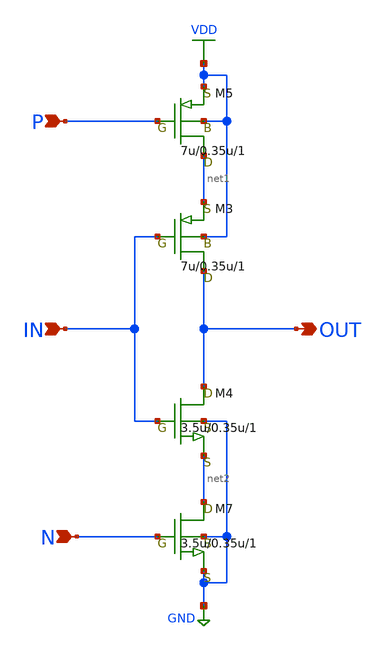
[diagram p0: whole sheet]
** sch_path: LR_hasegawa/LR_Work2/symbol/CLOCKEDINVERTER.sch
**.subckt CLOCKEDINVERTER OUT IN P N
*.opin OUT
*.ipin IN
*.ipin P
*.ipin N
M3 OUT IN net1 VDD pch w=7u l=0.35u as=0 ps=0 ad=0 pd=0 m=1
M4 OUT IN net2 GND nch w=3.5u l=0.35u as=0 ps=0 ad=0 pd=0 m=1
M5 net1 P VDD VDD pch w=7u l=0.35u as=1.05u ps=1.05u ad=3.7u pd=3.7u m=1
M7 net2 N GND GND nch w=3.5u l=0.35u as=0 ps=0 ad=0 pd=0 m=1
**.ends
.GLOBAL VDD
.GLOBAL GND
.end
